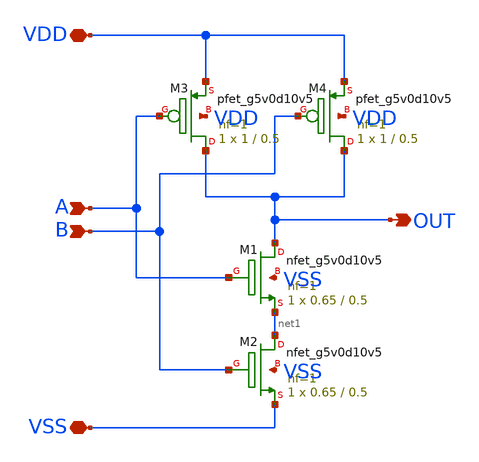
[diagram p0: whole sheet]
** sch_path: xschem/nand_gate.sch
**.subckt nand_gate VSS VDD B OUT A
*.iopin VSS
*.iopin VDD
*.ipin B
*.opin OUT
*.ipin A
XM2 net1 B VSS VSS sky130_fd_pr__nfet_g5v0d10v5 L=0.5 W=0.65 nf=1 ad='int((1 + 1)/2) * 0.65 / 1 * 0.29'
+ as='int((1 + 2)/2) * 0.65 / 1 * 0.29' pd='2*int((1 + 1)/2) * (0.65 / 1 + 0.29)' ps='2*int((1 + 2)/2) * (0.65 / 1 + 0.29)'
+ nrd='0.29 / 0.65 ' nrs='0.29 / 0.65 ' sa=0 sb=0 sd=0 mult=1 m=1
XM3 OUT A VDD VDD sky130_fd_pr__pfet_g5v0d10v5 L=0.5 W=1 nf=1 ad='int((1 + 1)/2) * 1 / 1 * 0.29' as='int((1 + 2)/2) * 1 / 1 * 0.29'
+ pd='2*int((1 + 1)/2) * (1 / 1 + 0.29)' ps='2*int((1 + 2)/2) * (1 / 1 + 0.29)' nrd='0.29 / 1 ' nrs='0.29 / 1 '
+ sa=0 sb=0 sd=0 mult=1 m=1
XM1 OUT A net1 VSS sky130_fd_pr__nfet_g5v0d10v5 L=0.5 W=0.65 nf=1 ad='int((1 + 1)/2) * 0.65 / 1 * 0.29'
+ as='int((1 + 2)/2) * 0.65 / 1 * 0.29' pd='2*int((1 + 1)/2) * (0.65 / 1 + 0.29)' ps='2*int((1 + 2)/2) * (0.65 / 1 + 0.29)'
+ nrd='0.29 / 0.65 ' nrs='0.29 / 0.65 ' sa=0 sb=0 sd=0 mult=1 m=1
XM4 OUT B VDD VDD sky130_fd_pr__pfet_g5v0d10v5 L=0.5 W=1 nf=1 ad='int((1 + 1)/2) * 1 / 1 * 0.29' as='int((1 + 2)/2) * 1 / 1 * 0.29'
+ pd='2*int((1 + 1)/2) * (1 / 1 + 0.29)' ps='2*int((1 + 2)/2) * (1 / 1 + 0.29)' nrd='0.29 / 1 ' nrs='0.29 / 1 '
+ sa=0 sb=0 sd=0 mult=1 m=1
**.ends
.end
